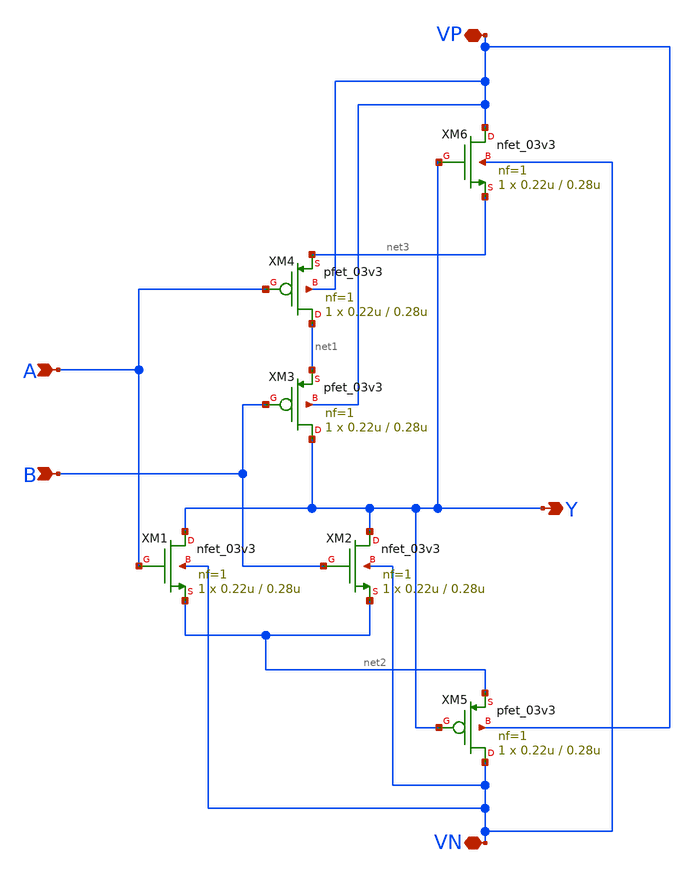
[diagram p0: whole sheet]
** sch_path: dls_nor.sch
**.subckt dls_nor VP B Y VN A
*.iopin VP
*.ipin B
*.opin Y
*.iopin VN
*.ipin A
XM1 Y A net2 VN nfet_03v3 L=0.28u W=0.22u nf=1 ad='int((nf+1)/2) * W/nf * 0.18u' as='int((nf+2)/2) * W/nf * 0.18u'
+ pd='2*int((nf+1)/2) * (W/nf + 0.18u)' ps='2*int((nf+2)/2) * (W/nf + 0.18u)' nrd='0.18u / W' nrs='0.18u / W'
+ sa=0 sb=0 sd=0 m=1
XM2 Y B net2 VN nfet_03v3 L=0.28u W=0.22u nf=1 ad='int((nf+1)/2) * W/nf * 0.18u' as='int((nf+2)/2) * W/nf * 0.18u'
+ pd='2*int((nf+1)/2) * (W/nf + 0.18u)' ps='2*int((nf+2)/2) * (W/nf + 0.18u)' nrd='0.18u / W' nrs='0.18u / W'
+ sa=0 sb=0 sd=0 m=1
XM3 Y B net1 VP pfet_03v3 L=0.28u W=0.22u nf=1 ad='int((nf+1)/2) * W/nf * 0.18u' as='int((nf+2)/2) * W/nf * 0.18u'
+ pd='2*int((nf+1)/2) * (W/nf + 0.18u)' ps='2*int((nf+2)/2) * (W/nf + 0.18u)' nrd='0.18u / W' nrs='0.18u / W'
+ sa=0 sb=0 sd=0 m=1
XM4 net1 A net3 VP pfet_03v3 L=0.28u W=0.22u nf=1 ad='int((nf+1)/2) * W/nf * 0.18u' as='int((nf+2)/2) * W/nf * 0.18u'
+ pd='2*int((nf+1)/2) * (W/nf + 0.18u)' ps='2*int((nf+2)/2) * (W/nf + 0.18u)' nrd='0.18u / W' nrs='0.18u / W'
+ sa=0 sb=0 sd=0 m=1
XM5 VN Y net2 VP pfet_03v3 L=0.28u W=0.22u nf=1 ad='int((nf+1)/2) * W/nf * 0.18u' as='int((nf+2)/2) * W/nf * 0.18u'
+ pd='2*int((nf+1)/2) * (W/nf + 0.18u)' ps='2*int((nf+2)/2) * (W/nf + 0.18u)' nrd='0.18u / W' nrs='0.18u / W'
+ sa=0 sb=0 sd=0 m=1
XM6 VP net4 net3 VN nfet_03v3 L=0.28u W=0.22u nf=1 ad='int((nf+1)/2) * W/nf * 0.18u' as='int((nf+2)/2) * W/nf * 0.18u'
+ pd='2*int((nf+1)/2) * (W/nf + 0.18u)' ps='2*int((nf+2)/2) * (W/nf + 0.18u)' nrd='0.18u / W' nrs='0.18u / W'
+ sa=0 sb=0 sd=0 m=1
**.ends
.end
